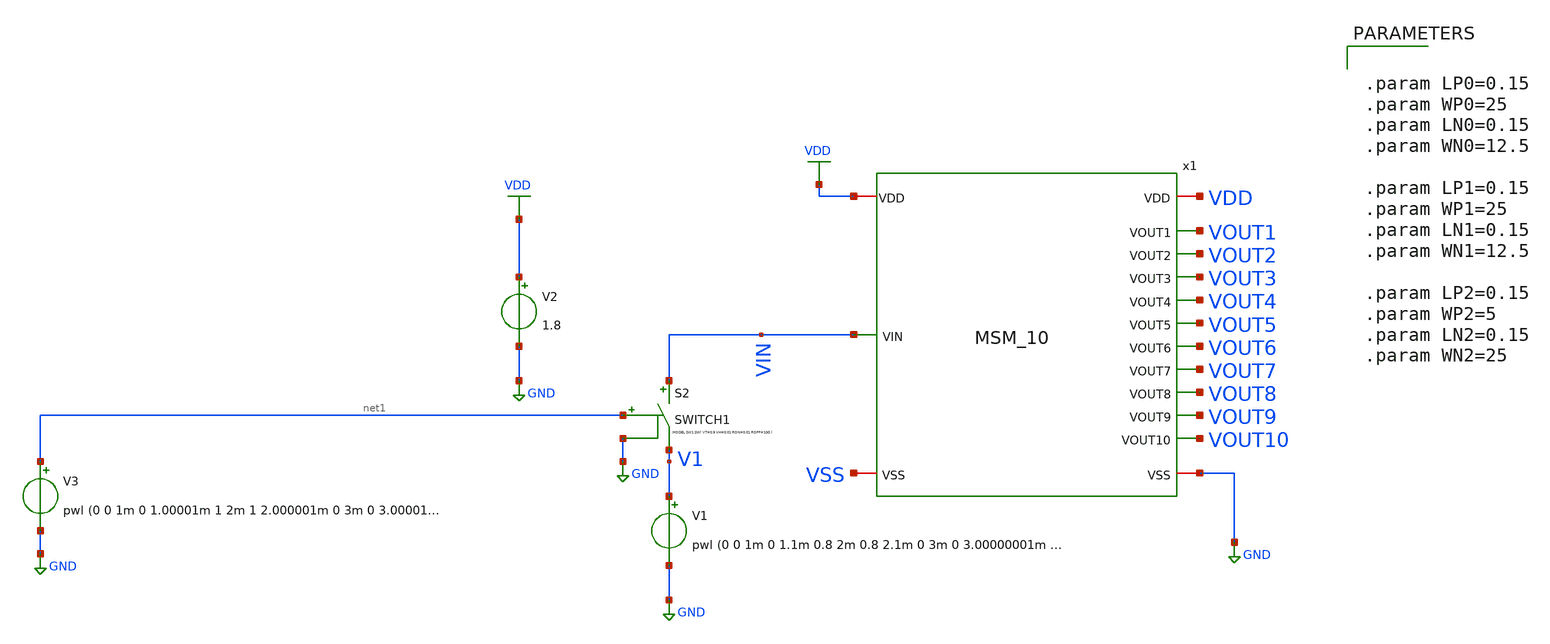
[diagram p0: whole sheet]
** sch_path: LIQAF circuit/10-Stage/Transient_MemoryTest.sch
**.subckt Transient_MemoryTest
V2 VDD GND 1.8
x1 VDD VOUT1 VOUT2 VIN VOUT3 VOUT4 VOUT5 VOUT6 VOUT7 VOUT8 VOUT9 VOUT10 GND MSM_10
V1 V1 GND pwl (0 0 1m 0 1.1m 0.8 2m 0.8 2.1m 0 3m 0 3.00000001m 0.9 4m 0.9 4.1m 0 5m 0)
S2 VIN V1 net1 GND SWITCH1
V3 net1 GND pwl (0 0 1m 0 1.00001m 1 2m 1 2.000001m 0 3m 0 3.00001m 1 4m 1 4.0000001m 0 5m 0)
**** begin user architecture code
 ** manual skywater pdks install (with patches applied)
* .lib $::SKYWATER_MODELS/models/sky130.lib.spice tt

** opencircuitdesign pdks install
.lib $::SKYWATER_MODELS/sky130.lib.spice tt

.param mc_mm_switch=0
.param mc_pr_switch=0


.tran 1u 5m
.control
run
plot v(VOUT1) v(VOUT2) v(VOUT3) v(VOUT4) v(VOUT5) v(VOUT6) v(VOUT7) v(VOUT8) v(VOUT9) v(VOUT10)
plot v(V1) v(VIN)
.endc
.save all



.param LP0=0.15
.param WP0=25
.param LN0=0.15
.param WN0=12.5

.param LP1=0.15
.param WP1=25
.param LN1=0.15
.param WN1=12.5

.param LP2=0.15
.param WP2=5
.param LN2=0.15
.param WN2=25


**** end user architecture code
**.ends
.GLOBAL GND
.GLOBAL VDD
.end
